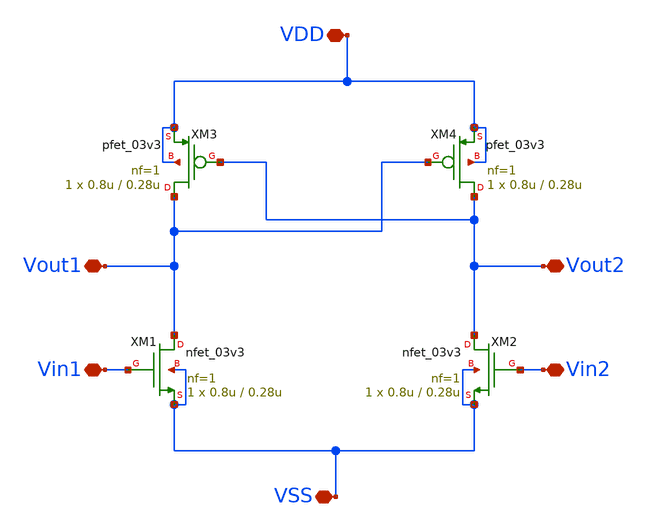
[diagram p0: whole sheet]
** sch_path: designs/comparator/rslatch.sch
**.subckt rslatch VDD VSS Vin1 Vin2 Vout1 Vout2
*.iopin VDD
*.iopin VSS
*.iopin Vin1
*.iopin Vin2
*.iopin Vout1
*.iopin Vout2
XM1 Vout1 Vin1 VSS VSS nfet_03v3 L=0.28u W=0.8u nf=1 ad='int((nf+1)/2) * W/nf * 0.18u' as='int((nf+2)/2) * W/nf * 0.18u'
+ pd='2*int((nf+1)/2) * (W/nf + 0.18u)' ps='2*int((nf+2)/2) * (W/nf + 0.18u)' nrd='0.18u / W' nrs='0.18u / W'
+ sa=0 sb=0 sd=0 m=1
XM2 Vout2 Vin2 VSS VSS nfet_03v3 L=0.28u W=0.8u nf=1 ad='int((nf+1)/2) * W/nf * 0.18u' as='int((nf+2)/2) * W/nf * 0.18u'
+ pd='2*int((nf+1)/2) * (W/nf + 0.18u)' ps='2*int((nf+2)/2) * (W/nf + 0.18u)' nrd='0.18u / W' nrs='0.18u / W'
+ sa=0 sb=0 sd=0 m=1
XM3 Vout1 Vout2 VDD VDD pfet_03v3 L=0.28u W=0.8u nf=1 ad='int((nf+1)/2) * W/nf * 0.18u' as='int((nf+2)/2) * W/nf * 0.18u'
+ pd='2*int((nf+1)/2) * (W/nf + 0.18u)' ps='2*int((nf+2)/2) * (W/nf + 0.18u)' nrd='0.18u / W' nrs='0.18u / W'
+ sa=0 sb=0 sd=0 m=1
XM4 Vout2 Vout1 VDD VDD pfet_03v3 L=0.28u W=0.8u nf=1 ad='int((nf+1)/2) * W/nf * 0.18u' as='int((nf+2)/2) * W/nf * 0.18u'
+ pd='2*int((nf+1)/2) * (W/nf + 0.18u)' ps='2*int((nf+2)/2) * (W/nf + 0.18u)' nrd='0.18u / W' nrs='0.18u / W'
+ sa=0 sb=0 sd=0 m=1
**.ends
.end
